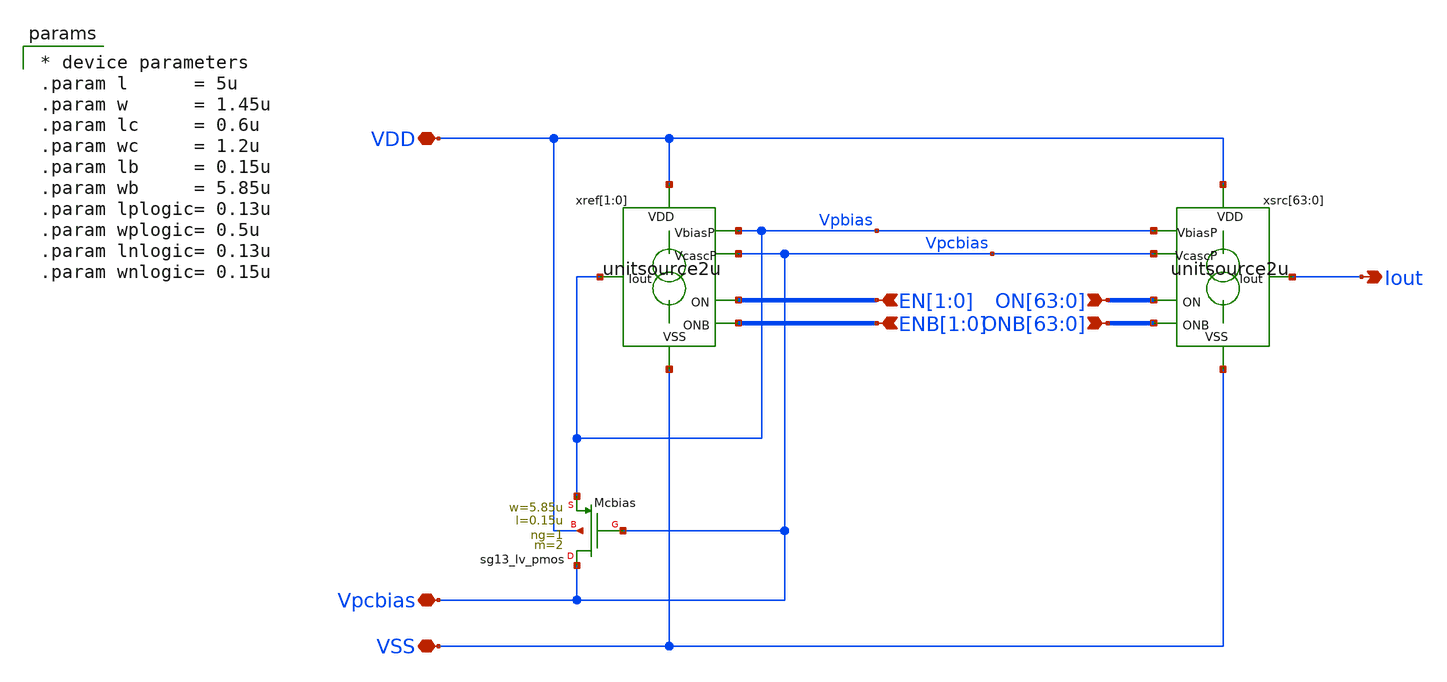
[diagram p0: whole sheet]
** sch_path: xschem/dac2u64out2in.sch
**.subckt dac2u64out2in Iout
*+ ON[63],ON[62],ON[61],ON[60],ON[59],ON[58],ON[57],ON[56],ON[55],ON[54],ON[53],ON[52],ON[51],ON[50],ON[49],ON[48],ON[47],ON[46],ON[45],ON[44],ON[43],ON[42],ON[41],ON[40],ON[39],ON[38],ON[37],ON[36],ON[35],ON[34],ON[33],ON[32],ON[31],ON[30],ON[29],ON[28],ON[27],ON[26],ON[25],ON[24],ON[23],ON[22],ON[21],ON[20],ON[19],ON[18],ON[17],ON[16],ON[15],ON[14],ON[13],ON[12],ON[11],ON[10],ON[9],ON[8],ON[7],ON[6],ON[5],ON[4],ON[3],ON[2],ON[1],ON[0]
*+ ONB[63],ONB[62],ONB[61],ONB[60],ONB[59],ONB[58],ONB[57],ONB[56],ONB[55],ONB[54],ONB[53],ONB[52],ONB[51],ONB[50],ONB[49],ONB[48],ONB[47],ONB[46],ONB[45],ONB[44],ONB[43],ONB[42],ONB[41],ONB[40],ONB[39],ONB[38],ONB[37],ONB[36],ONB[35],ONB[34],ONB[33],ONB[32],ONB[31],ONB[30],ONB[29],ONB[28],ONB[27],ONB[26],ONB[25],ONB[24],ONB[23],ONB[22],ONB[21],ONB[20],ONB[19],ONB[18],ONB[17],ONB[16],ONB[15],ONB[14],ONB[13],ONB[12],ONB[11],ONB[10],ONB[9],ONB[8],ONB[7],ONB[6],ONB[5],ONB[4],ONB[3],ONB[2],ONB[1],ONB[0] VSS VDD Vpcbias EN[1],EN[0] ENB[1],ENB[0]
*.opin Iout
*.ipin
*+ ON[63],ON[62],ON[61],ON[60],ON[59],ON[58],ON[57],ON[56],ON[55],ON[54],ON[53],ON[52],ON[51],ON[50],ON[49],ON[48],ON[47],ON[46],ON[45],ON[44],ON[43],ON[42],ON[41],ON[40],ON[39],ON[38],ON[37],ON[36],ON[35],ON[34],ON[33],ON[32],ON[31],ON[30],ON[29],ON[28],ON[27],ON[26],ON[25],ON[24],ON[23],ON[22],ON[21],ON[20],ON[19],ON[18],ON[17],ON[16],ON[15],ON[14],ON[13],ON[12],ON[11],ON[10],ON[9],ON[8],ON[7],ON[6],ON[5],ON[4],ON[3],ON[2],ON[1],ON[0]
*.ipin
*+ ONB[63],ONB[62],ONB[61],ONB[60],ONB[59],ONB[58],ONB[57],ONB[56],ONB[55],ONB[54],ONB[53],ONB[52],ONB[51],ONB[50],ONB[49],ONB[48],ONB[47],ONB[46],ONB[45],ONB[44],ONB[43],ONB[42],ONB[41],ONB[40],ONB[39],ONB[38],ONB[37],ONB[36],ONB[35],ONB[34],ONB[33],ONB[32],ONB[31],ONB[30],ONB[29],ONB[28],ONB[27],ONB[26],ONB[25],ONB[24],ONB[23],ONB[22],ONB[21],ONB[20],ONB[19],ONB[18],ONB[17],ONB[16],ONB[15],ONB[14],ONB[13],ONB[12],ONB[11],ONB[10],ONB[9],ONB[8],ONB[7],ONB[6],ONB[5],ONB[4],ONB[3],ONB[2],ONB[1],ONB[0]
*.iopin VSS
*.iopin VDD
*.iopin Vpcbias
*.ipin EN[1],EN[0]
*.ipin ENB[1],ENB[0]
XMcbias Vpcbias Vpcbias Vpbias VDD sg13_lv_pmos w=5.85u l=0.15u ng=1 m=2 mm_ok=1
xref[1] VDD Vpbias EN[1] ENB[1] Vpbias Vpcbias VSS unitsource2u
xref[0] VDD Vpbias EN[0] ENB[0] Vpbias Vpcbias VSS unitsource2u
xsrc[63] VDD Vpbias ON[63] ONB[63] Iout Vpcbias VSS unitsource2u
xsrc[62] VDD Vpbias ON[62] ONB[62] Iout Vpcbias VSS unitsource2u
xsrc[61] VDD Vpbias ON[61] ONB[61] Iout Vpcbias VSS unitsource2u
xsrc[60] VDD Vpbias ON[60] ONB[60] Iout Vpcbias VSS unitsource2u
xsrc[59] VDD Vpbias ON[59] ONB[59] Iout Vpcbias VSS unitsource2u
xsrc[58] VDD Vpbias ON[58] ONB[58] Iout Vpcbias VSS unitsource2u
xsrc[57] VDD Vpbias ON[57] ONB[57] Iout Vpcbias VSS unitsource2u
xsrc[56] VDD Vpbias ON[56] ONB[56] Iout Vpcbias VSS unitsource2u
xsrc[55] VDD Vpbias ON[55] ONB[55] Iout Vpcbias VSS unitsource2u
xsrc[54] VDD Vpbias ON[54] ONB[54] Iout Vpcbias VSS unitsource2u
xsrc[53] VDD Vpbias ON[53] ONB[53] Iout Vpcbias VSS unitsource2u
xsrc[52] VDD Vpbias ON[52] ONB[52] Iout Vpcbias VSS unitsource2u
xsrc[51] VDD Vpbias ON[51] ONB[51] Iout Vpcbias VSS unitsource2u
xsrc[50] VDD Vpbias ON[50] ONB[50] Iout Vpcbias VSS unitsource2u
xsrc[49] VDD Vpbias ON[49] ONB[49] Iout Vpcbias VSS unitsource2u
xsrc[48] VDD Vpbias ON[48] ONB[48] Iout Vpcbias VSS unitsource2u
xsrc[47] VDD Vpbias ON[47] ONB[47] Iout Vpcbias VSS unitsource2u
xsrc[46] VDD Vpbias ON[46] ONB[46] Iout Vpcbias VSS unitsource2u
xsrc[45] VDD Vpbias ON[45] ONB[45] Iout Vpcbias VSS unitsource2u
xsrc[44] VDD Vpbias ON[44] ONB[44] Iout Vpcbias VSS unitsource2u
xsrc[43] VDD Vpbias ON[43] ONB[43] Iout Vpcbias VSS unitsource2u
xsrc[42] VDD Vpbias ON[42] ONB[42] Iout Vpcbias VSS unitsource2u
xsrc[41] VDD Vpbias ON[41] ONB[41] Iout Vpcbias VSS unitsource2u
xsrc[40] VDD Vpbias ON[40] ONB[40] Iout Vpcbias VSS unitsource2u
xsrc[39] VDD Vpbias ON[39] ONB[39] Iout Vpcbias VSS unitsource2u
xsrc[38] VDD Vpbias ON[38] ONB[38] Iout Vpcbias VSS unitsource2u
xsrc[37] VDD Vpbias ON[37] ONB[37] Iout Vpcbias VSS unitsource2u
xsrc[36] VDD Vpbias ON[36] ONB[36] Iout Vpcbias VSS unitsource2u
xsrc[35] VDD Vpbias ON[35] ONB[35] Iout Vpcbias VSS unitsource2u
xsrc[34] VDD Vpbias ON[34] ONB[34] Iout Vpcbias VSS unitsource2u
xsrc[33] VDD Vpbias ON[33] ONB[33] Iout Vpcbias VSS unitsource2u
xsrc[32] VDD Vpbias ON[32] ONB[32] Iout Vpcbias VSS unitsource2u
xsrc[31] VDD Vpbias ON[31] ONB[31] Iout Vpcbias VSS unitsource2u
xsrc[30] VDD Vpbias ON[30] ONB[30] Iout Vpcbias VSS unitsource2u
xsrc[29] VDD Vpbias ON[29] ONB[29] Iout Vpcbias VSS unitsource2u
xsrc[28] VDD Vpbias ON[28] ONB[28] Iout Vpcbias VSS unitsource2u
xsrc[27] VDD Vpbias ON[27] ONB[27] Iout Vpcbias VSS unitsource2u
xsrc[26] VDD Vpbias ON[26] ONB[26] Iout Vpcbias VSS unitsource2u
xsrc[25] VDD Vpbias ON[25] ONB[25] Iout Vpcbias VSS unitsource2u
xsrc[24] VDD Vpbias ON[24] ONB[24] Iout Vpcbias VSS unitsource2u
xsrc[23] VDD Vpbias ON[23] ONB[23] Iout Vpcbias VSS unitsource2u
xsrc[22] VDD Vpbias ON[22] ONB[22] Iout Vpcbias VSS unitsource2u
xsrc[21] VDD Vpbias ON[21] ONB[21] Iout Vpcbias VSS unitsource2u
xsrc[20] VDD Vpbias ON[20] ONB[20] Iout Vpcbias VSS unitsource2u
xsrc[19] VDD Vpbias ON[19] ONB[19] Iout Vpcbias VSS unitsource2u
xsrc[18] VDD Vpbias ON[18] ONB[18] Iout Vpcbias VSS unitsource2u
xsrc[17] VDD Vpbias ON[17] ONB[17] Iout Vpcbias VSS unitsource2u
xsrc[16] VDD Vpbias ON[16] ONB[16] Iout Vpcbias VSS unitsource2u
xsrc[15] VDD Vpbias ON[15] ONB[15] Iout Vpcbias VSS unitsource2u
xsrc[14] VDD Vpbias ON[14] ONB[14] Iout Vpcbias VSS unitsource2u
xsrc[13] VDD Vpbias ON[13] ONB[13] Iout Vpcbias VSS unitsource2u
xsrc[12] VDD Vpbias ON[12] ONB[12] Iout Vpcbias VSS unitsource2u
xsrc[11] VDD Vpbias ON[11] ONB[11] Iout Vpcbias VSS unitsource2u
xsrc[10] VDD Vpbias ON[10] ONB[10] Iout Vpcbias VSS unitsource2u
xsrc[9] VDD Vpbias ON[9] ONB[9] Iout Vpcbias VSS unitsource2u
xsrc[8] VDD Vpbias ON[8] ONB[8] Iout Vpcbias VSS unitsource2u
xsrc[7] VDD Vpbias ON[7] ONB[7] Iout Vpcbias VSS unitsource2u
xsrc[6] VDD Vpbias ON[6] ONB[6] Iout Vpcbias VSS unitsource2u
xsrc[5] VDD Vpbias ON[5] ONB[5] Iout Vpcbias VSS unitsource2u
xsrc[4] VDD Vpbias ON[4] ONB[4] Iout Vpcbias VSS unitsource2u
xsrc[3] VDD Vpbias ON[3] ONB[3] Iout Vpcbias VSS unitsource2u
xsrc[2] VDD Vpbias ON[2] ONB[2] Iout Vpcbias VSS unitsource2u
xsrc[1] VDD Vpbias ON[1] ONB[1] Iout Vpcbias VSS unitsource2u
xsrc[0] VDD Vpbias ON[0] ONB[0] Iout Vpcbias VSS unitsource2u
**** begin user architecture code

* device parameters
.param l      = 5u
.param w      = 1.45u
.param lc     = 0.6u
.param wc     = 1.2u
.param lb     = 0.15u
.param wb     = 5.85u
.param lplogic= 0.13u
.param wplogic= 0.5u
.param lnlogic= 0.13u
.param wnlogic= 0.15u


**** end user architecture code
**.ends

* expanding   symbol:  unitsource2u.sym # of pins=7
** sym_path: xschem/unitsource2u.sym
** sch_path: xschem/unitsource2u.sch
.subckt unitsource2u VDD VbiasP ON ONB Iout VcascP VSS
*.iopin VSS
*.iopin VDD
*.iopin VbiasP
*.iopin VcascP
*.ipin ON
*.ipin ONB
*.iopin Iout
xnonoverlap VDD VSS ON ONB on_n off_n nonoverlap
xsw VDD off_n Vcasc on_n VcascP cascodeswitch_pmos
xsrc VDD VbiasP Vcasc Iout pcsource2u
.ends


* expanding   symbol:  nonoverlap.sym # of pins=6
** sym_path: xschem/nonoverlap.sym
** sch_path: xschem/nonoverlap.sch
.subckt nonoverlap VDD VSS INP INN OUTN OUTP
*.iopin VSS
*.iopin VDD
*.ipin INP
*.ipin INN
*.opin OUTP
*.opin OUTN
XM1 OUTN INP VDD VDD sg13_lv_pmos w=0.3u l=0.13u ng=1 m=1 mm_ok=1
XM2 OUTP INN VDD VDD sg13_lv_pmos w=0.3u l=0.13u ng=1 m=1 mm_ok=1
XM3 OUTN OUTP VSS VSS sg13_lv_nmos w=0.15u l=0.52u ng=1 m=1 mm_ok=1
XM4 OUTP OUTN VSS VSS sg13_lv_nmos w=0.15u l=0.52u ng=1 m=1 mm_ok=1
.ends


* expanding   symbol:  cascodeswitch_pmos.sym # of pins=5
** sym_path: xschem/cascodeswitch_pmos.sym
** sch_path: xschem/cascodeswitch_pmos.sch
.subckt cascodeswitch_pmos VDD off_n Vcasc on_n Vbpcasc
*.ipin off_n
*.ipin Vbpcasc
*.opin Vcasc
*.ipin on_n
*.ipin VDD
XMpullup Vcasc off_n VDD VDD sg13_lv_pmos w=0.3u l=0.13u ng=1 m=1 mm_ok=1
XMbias Vbpcasc on_n Vcasc VDD sg13_lv_pmos w=0.3u l=0.13u ng=1 m=1 mm_ok=1
.ends


* expanding   symbol:  pcsource2u.sym # of pins=4
** sym_path: xschem/pcsource2u.sym
** sch_path: xschem/pcsource2u.sch
.subckt pcsource2u VDD VbiasP VcascodeP Iout
*.ipin VcascodeP
*.ipin VbiasP
*.opin Iout
*.ipin VDD
XMsrc drain net4 VDD net1 sg13_lv_pmos w=1.45u l=5u ng=1 m=1 mm_ok=1
XMcasc Iout net3 drain net2 sg13_lv_pmos w=1.2u l=0.6u ng=1 m=1 mm_ok=1
Vgsrc net4 VbiasP 0
.save i(vgsrc)
Vgcasc net3 VcascodeP 0
.save i(vgcasc)
Vbsrc VDD net1 0
.save i(vbsrc)
Vbcasc VDD net2 0
.save i(vbcasc)
.ends

.end
